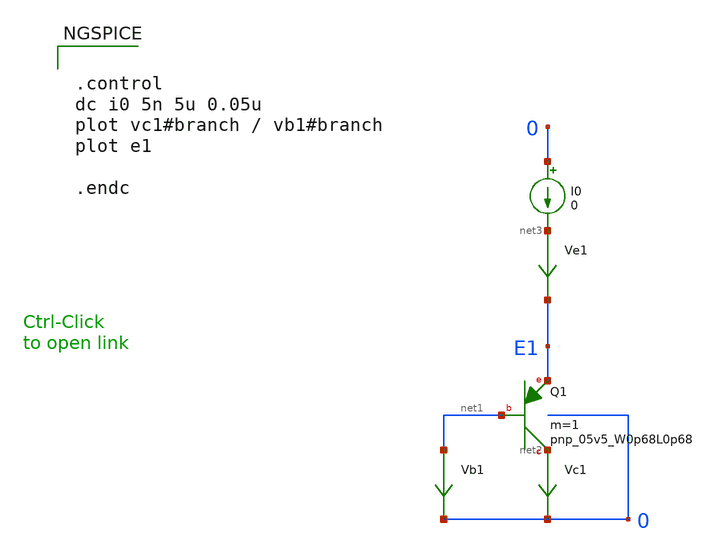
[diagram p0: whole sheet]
** sch_path: sky130_tests_ng/test_bipolar.sch
* Copyright 2020 Stefan Frederik Schippers
* Licensed under the Apache License, Version 2.0 (the "License");
* you may not use this file except in compliance with the License.
* You may obtain a copy of the License at
* https://www.apache.org/licenses/LICENSE-2.0
* Unless required by applicable law or agreed to in writing, software
* distributed under the License is distributed on an "AS IS" BASIS,
* WITHOUT WARRANTIES OR CONDITIONS OF ANY KIND, either express or implied.
* See the License for the specific language governing permissions and
* limitations under the License.
**.subckt test_bipolar
XQ1 net2 net1 E1 sky130_fd_pr__pnp_05v5_W0p68L0p68 m=1
Vc1 net2 0 0
.save i(vc1)
Vb1 net1 0 0
.save i(vb1)
I0 0 net3 0
Ve1 net3 E1 0
.save i(ve1)
**** begin user architecture code


.control
dc i0 5n 5u 0.05u
plot vc1#branch / vb1#branch
plot e1

.endc



**** end user architecture code
**.ends
.end
